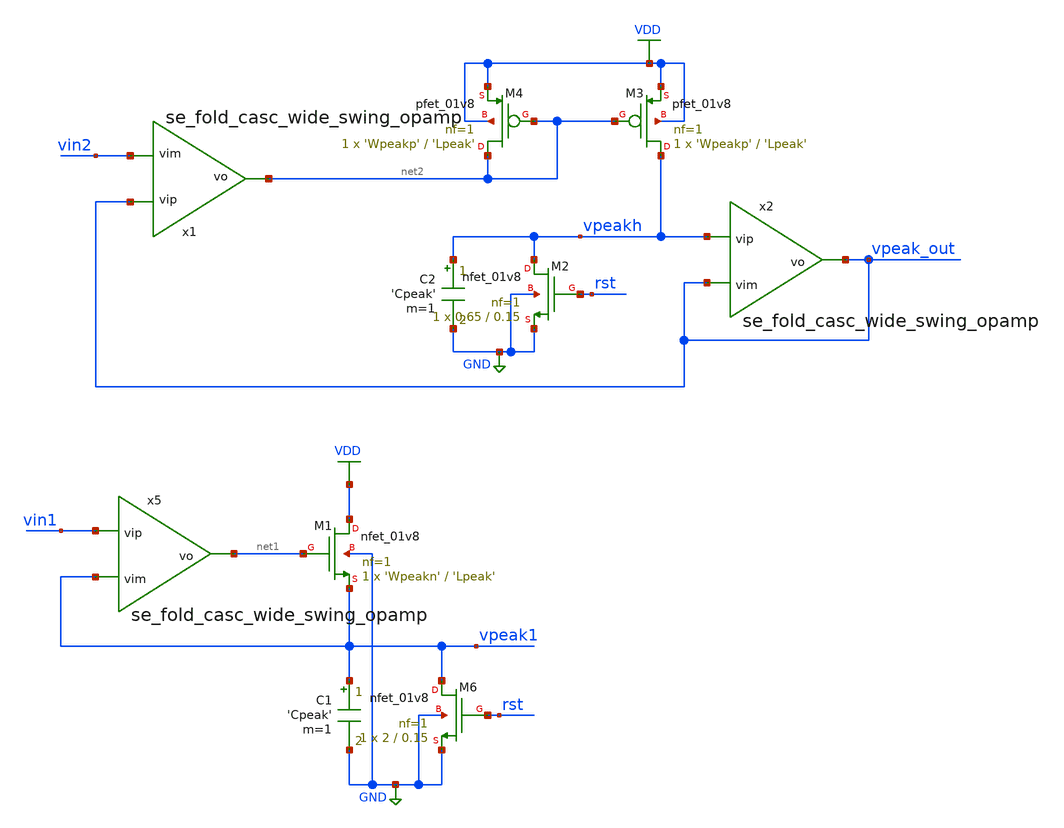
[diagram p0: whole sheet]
** sch_path: designs/peak_detector.sch
* Copyright 2020 Stefan Frederik Schippers
* Licensed under the Apache License, Version 2.0 (the "License");
* you may not use this file except in compliance with the License.
* You may obtain a copy of the License at
* https://www.apache.org/licenses/LICENSE-2.0
* Unless required by applicable law or agreed to in writing, software
* distributed under the License is distributed on an "AS IS" BASIS,
* WITHOUT WARRANTIES OR CONDITIONS OF ANY KIND, either express or implied.
* See the License for the specific language governing permissions and
* limitations under the License.
**.subckt peak_detector
x5 net1 vin1 vpeak1 se_fold_casc_wide_swing_opamp Lbias=6.4 Ibias=10u
C1 vpeak1 GND 'Cpeak' m=1
XM6 vpeak1 rst GND GND sky130_fd_pr__nfet_01v8 L=0.15 W=2 nf=1 ad='int((nf+1)/2) * W/nf * 0.29' as='int((nf+2)/2) * W/nf * 0.29'
+ pd='2*int((nf+1)/2) * (W/nf + 0.29)' ps='2*int((nf+2)/2) * (W/nf + 0.29)' nrd='0.29 / W' nrs='0.29 / W'
+ sa=0 sb=0 sd=0 mult=1 m=1
XM1 VDD net1 vpeak1 GND sky130_fd_pr__nfet_01v8 L='Lpeak' W='Wpeakn' nf=1 ad='int((nf+1)/2) * W/nf * 0.29'
+ as='int((nf+2)/2) * W/nf * 0.29' pd='2*int((nf+1)/2) * (W/nf + 0.29)' ps='2*int((nf+2)/2) * (W/nf + 0.29)'
+ nrd='0.29 / W' nrs='0.29 / W' sa=0 sb=0 sd=0 mult=1 m=1
x1 net2 vpeak_out vin2 se_fold_casc_wide_swing_opamp Lbias=6.4 Ibias=10u
C2 vpeakh GND 'Cpeak' m=1
XM3 vpeakh net2 VDD VDD sky130_fd_pr__pfet_01v8 L='Lpeak' W='Wpeakp' nf=1 ad='int((nf+1)/2) * W/nf * 0.29'
+ as='int((nf+2)/2) * W/nf * 0.29' pd='2*int((nf+1)/2) * (W/nf + 0.29)' ps='2*int((nf+2)/2) * (W/nf + 0.29)'
+ nrd='0.29 / W' nrs='0.29 / W' sa=0 sb=0 sd=0 mult=1 m=1
XM4 net2 net2 VDD VDD sky130_fd_pr__pfet_01v8 L='Lpeak' W='Wpeakp' nf=1 ad='int((nf+1)/2) * W/nf * 0.29'
+ as='int((nf+2)/2) * W/nf * 0.29' pd='2*int((nf+1)/2) * (W/nf + 0.29)' ps='2*int((nf+2)/2) * (W/nf + 0.29)'
+ nrd='0.29 / W' nrs='0.29 / W' sa=0 sb=0 sd=0 mult=1 m=1
x2 vpeak_out vpeakh vpeak_out se_fold_casc_wide_swing_opamp Lbias=6.4 Ibias=10u
XM2 vpeakh rst GND GND sky130_fd_pr__nfet_01v8 L=0.15 W=0.65 nf=1 ad='int((nf+1)/2) * W/nf * 0.29' as='int((nf+2)/2) * W/nf * 0.29'
+ pd='2*int((nf+1)/2) * (W/nf + 0.29)' ps='2*int((nf+2)/2) * (W/nf + 0.29)' nrd='0.29 / W' nrs='0.29 / W'
+ sa=0 sb=0 sd=0 mult=1 m=1
**** begin user architecture code

.include $::SKYWATER_MODELS/cells/nfet_01v8/sky130_fd_pr__nfet_01v8__tt.corner.spice
.include $::SKYWATER_MODELS/cells/nfet_01v8_lvt/sky130_fd_pr__nfet_01v8_lvt__tt.corner.spice
.include $::SKYWATER_MODELS/cells/pfet_01v8/sky130_fd_pr__pfet_01v8__tt.corner.spice
.include $::SKYWATER_MODELS/cells/nfet_03v3_nvt/sky130_fd_pr__nfet_03v3_nvt__tt.corner.spice
.include $::SKYWATER_MODELS/cells/nfet_05v0_nvt/sky130_fd_pr__nfet_05v0_nvt__tt.corner.spice
.include $::SKYWATER_MODELS/cells/esd_nfet_01v8/sky130_fd_pr__esd_nfet_01v8__tt.corner.spice
.include $::SKYWATER_MODELS/cells/pfet_01v8_lvt/sky130_fd_pr__pfet_01v8_lvt__tt.corner.spice
.include $::SKYWATER_MODELS/cells/pfet_01v8_hvt/sky130_fd_pr__pfet_01v8_hvt__tt.corner.spice
.include $::SKYWATER_MODELS/cells/esd_pfet_g5v0d10v5/sky130_fd_pr__esd_pfet_g5v0d10v5__tt.corner.spice
.include $::SKYWATER_MODELS/cells/pfet_g5v0d10v5/sky130_fd_pr__pfet_g5v0d10v5__tt.corner.spice
.include $::SKYWATER_MODELS/cells/pfet_g5v0d16v0/sky130_fd_pr__pfet_g5v0d16v0__tt.corner.spice
.include $::SKYWATER_MODELS/cells/nfet_g5v0d10v5/sky130_fd_pr__nfet_g5v0d10v5__tt.corner.spice
.include $::SKYWATER_MODELS/cells/nfet_g5v0d16v0/sky130_fd_pr__nfet_g5v0d16v0__tt_discrete.corner.spice
.include $::SKYWATER_MODELS/cells/esd_nfet_g5v0d10v5/sky130_fd_pr__esd_nfet_g5v0d10v5__tt.corner.spice
.include $::SKYWATER_MODELS/models/corners/tt/nonfet.spice
* Mismatch parameters
.include $::SKYWATER_MODELS/cells/nfet_01v8/sky130_fd_pr__nfet_01v8__mismatch.corner.spice
.include $::SKYWATER_MODELS/cells/pfet_01v8/sky130_fd_pr__pfet_01v8__mismatch.corner.spice
.include $::SKYWATER_MODELS/cells/nfet_01v8_lvt/sky130_fd_pr__nfet_01v8_lvt__mismatch.corner.spice
.include $::SKYWATER_MODELS/cells/pfet_01v8_lvt/sky130_fd_pr__pfet_01v8_lvt__mismatch.corner.spice
.include $::SKYWATER_MODELS/cells/pfet_01v8_hvt/sky130_fd_pr__pfet_01v8_hvt__mismatch.corner.spice
.include $::SKYWATER_MODELS/cells/nfet_g5v0d10v5/sky130_fd_pr__nfet_g5v0d10v5__mismatch.corner.spice
.include $::SKYWATER_MODELS/cells/pfet_g5v0d10v5/sky130_fd_pr__pfet_g5v0d10v5__mismatch.corner.spice
.include $::SKYWATER_MODELS/cells/nfet_05v0_nvt/sky130_fd_pr__nfet_05v0_nvt__mismatch.corner.spice
.include $::SKYWATER_MODELS/cells/nfet_03v3_nvt/sky130_fd_pr__nfet_03v3_nvt__mismatch.corner.spice
* Resistor$::SKYWATER_MODELS/Capacitor
.include $::SKYWATER_MODELS/models/r+c/res_typical__cap_typical.spice
.include $::SKYWATER_MODELS/models/r+c/res_typical__cap_typical__lin.spice
* Special cells
.include $::SKYWATER_MODELS/models/corners/tt/specialized_cells.spice
* All models
.include $::SKYWATER_MODELS/models/all.spice
* Corner
.include $::SKYWATER_MODELS/models/corners/tt/rf.spice

**** end user architecture code
**.ends

* expanding   symbol:
*+  /home/users/nhpoole/ee272b/ee272b_mixed_signal_mmwave_accelerator/designs/se_fold_casc_wide_swing_opamp.sym # of pins=3
** sym_path: designs/se_fold_casc_wide_swing_opamp.sym
** sch_path: designs/se_fold_casc_wide_swing_opamp.sch
.subckt se_fold_casc_wide_swing_opamp vo vip vim  Lbias=6.4 Ibias=10u
*.ipin vip
*.ipin vim
*.opin vo
V6 vtail_cascn net1 0
XM7 net1 vbias4 GND GND sky130_fd_pr__nfet_01v8 L='Lbias*nfactorL' W='Wbias*nfactorW' nf=1 ad='int((nf+1)/2) * W/nf * 0.29'
+ as='int((nf+2)/2) * W/nf * 0.29' pd='2*int((nf+1)/2) * (W/nf + 0.29)' ps='2*int((nf+2)/2) * (W/nf + 0.29)'
+ nrd='0.29 / W' nrs='0.29 / W' sa=0 sb=0 sd=0 mult='9*K' m='9*K'
XM10 vcascnp vbias4 GND GND sky130_fd_pr__nfet_01v8 L='Lbias*nfactorL' W='2*Wbias*nfactorW' nf=1 ad='int((nf+1)/2) * W/nf * 0.29'
+ as='int((nf+2)/2) * W/nf * 0.29' pd='2*int((nf+1)/2) * (W/nf + 0.29)' ps='2*int((nf+2)/2) * (W/nf + 0.29)'
+ nrd='0.29 / W' nrs='0.29 / W' sa=0 sb=0 sd=0 mult='9*K' m='9*K'
XM11 net11 vbias3 vcascnp GND sky130_fd_pr__nfet_01v8 L='Lbias*nfactorL' W='Wbias*nfactorW' nf=1 ad='int((nf+1)/2) * W/nf * 0.29'
+ as='int((nf+2)/2) * W/nf * 0.29' pd='2*int((nf+1)/2) * (W/nf + 0.29)' ps='2*int((nf+2)/2) * (W/nf + 0.29)'
+ nrd='0.29 / W' nrs='0.29 / W' sa=0 sb=0 sd=0 mult='9*K' m='9*K'
XM27 vcascnm vbias4 GND GND sky130_fd_pr__nfet_01v8 L='Lbias*nfactorL' W='2*Wbias*nfactorW' nf=1 ad='int((nf+1)/2) * W/nf * 0.29'
+ as='int((nf+2)/2) * W/nf * 0.29' pd='2*int((nf+1)/2) * (W/nf + 0.29)' ps='2*int((nf+2)/2) * (W/nf + 0.29)'
+ nrd='0.29 / W' nrs='0.29 / W' sa=0 sb=0 sd=0 mult='9*K' m='9*K'
XM28 vo vbias3 vcascnm GND sky130_fd_pr__nfet_01v8 L='Lbias*nfactorL' W='Wbias*nfactorW' nf=1 ad='int((nf+1)/2) * W/nf * 0.29'
+ as='int((nf+2)/2) * W/nf * 0.29' pd='2*int((nf+1)/2) * (W/nf + 0.29)' ps='2*int((nf+2)/2) * (W/nf + 0.29)'
+ nrd='0.29 / W' nrs='0.29 / W' sa=0 sb=0 sd=0 mult='9*K' m='9*K'
XM36 vbias1 vbias2 net7 VDD sky130_fd_pr__pfet_01v8 L='Lbias' W='2*Wbias' nf=1 ad='int((nf+1)/2) * W/nf * 0.29'
+ as='int((nf+2)/2) * W/nf * 0.29' pd='2*int((nf+1)/2) * (W/nf + 0.29)' ps='2*int((nf+2)/2) * (W/nf + 0.29)'
+ nrd='0.29 / W' nrs='0.29 / W' sa=0 sb=0 sd=0 mult='9*K' m='9*K'
XM37 net4 vbias2 net2 VDD sky130_fd_pr__pfet_01v8 L='Lbias' W='2*Wbias' nf=1 ad='int((nf+1)/2) * W/nf * 0.29'
+ as='int((nf+2)/2) * W/nf * 0.29' pd='2*int((nf+1)/2) * (W/nf + 0.29)' ps='2*int((nf+2)/2) * (W/nf + 0.29)'
+ nrd='0.29 / W' nrs='0.29 / W' sa=0 sb=0 sd=0 mult='9*K' m='9*K'
XM38 net6 vbias2 net5 VDD sky130_fd_pr__pfet_01v8 L='Lbias' W='2*Wbias' nf=1 ad='int((nf+1)/2) * W/nf * 0.29'
+ as='int((nf+2)/2) * W/nf * 0.29' pd='2*int((nf+1)/2) * (W/nf + 0.29)' ps='2*int((nf+2)/2) * (W/nf + 0.29)'
+ nrd='0.29 / W' nrs='0.29 / W' sa=0 sb=0 sd=0 mult='9*K' m='9*K'
XM39 vbias2 net3 vbias1 VDD sky130_fd_pr__pfet_01v8 L='Lbias' W='Wbias' nf=1 ad='int((nf+1)/2) * W/nf * 0.29'
+ as='int((nf+2)/2) * W/nf * 0.29' pd='2*int((nf+1)/2) * (W/nf + 0.29)' ps='2*int((nf+2)/2) * (W/nf + 0.29)'
+ nrd='0.29 / W' nrs='0.29 / W' sa=0 sb=0 sd=0 mult='3*K' m='3*K'
XM40 net3 net3 vbias2 VDD sky130_fd_pr__pfet_01v8 L='Lbias' W='3*Wbias' nf=1 ad='int((nf+1)/2) * W/nf * 0.29'
+ as='int((nf+2)/2) * W/nf * 0.29' pd='2*int((nf+1)/2) * (W/nf + 0.29)' ps='2*int((nf+2)/2) * (W/nf + 0.29)'
+ nrd='0.29 / W' nrs='0.29 / W' sa=0 sb=0 sd=0 mult='9*K' m='9*K'
XM41 net4 net4 vbias3 GND sky130_fd_pr__nfet_01v8 L='Lbias*nfactorL' W='3*Wbias*nfactorW' nf=1 ad='int((nf+1)/2) * W/nf * 0.29'
+ as='int((nf+2)/2) * W/nf * 0.29' pd='2*int((nf+1)/2) * (W/nf + 0.29)' ps='2*int((nf+2)/2) * (W/nf + 0.29)'
+ nrd='0.29 / W' nrs='0.29 / W' sa=0 sb=0 sd=0 mult='9*K' m='9*K'
XM42 vbias3 net4 vbias4 GND sky130_fd_pr__nfet_01v8 L='Lbias*nfactorL' W='Wbias*nfactorW' nf=1 ad='int((nf+1)/2) * W/nf * 0.29'
+ as='int((nf+2)/2) * W/nf * 0.29' pd='2*int((nf+1)/2) * (W/nf + 0.29)' ps='2*int((nf+2)/2) * (W/nf + 0.29)'
+ nrd='0.29 / W' nrs='0.29 / W' sa=0 sb=0 sd=0 mult='K' m='K'
XM43 vbias4 vbias3 net9 GND sky130_fd_pr__nfet_01v8 L='Lbias*nfactorL' W='Wbias*nfactorW' nf=1 ad='int((nf+1)/2) * W/nf * 0.29'
+ as='int((nf+2)/2) * W/nf * 0.29' pd='2*int((nf+1)/2) * (W/nf + 0.29)' ps='2*int((nf+2)/2) * (W/nf + 0.29)'
+ nrd='0.29 / W' nrs='0.29 / W' sa=0 sb=0 sd=0 mult='9*K' m='9*K'
XM44 net10 vbias4 GND GND sky130_fd_pr__nfet_01v8 L='Lbias*nfactorL' W='Wbias*nfactorW' nf=1 ad='int((nf+1)/2) * W/nf * 0.29'
+ as='int((nf+2)/2) * W/nf * 0.29' pd='2*int((nf+1)/2) * (W/nf + 0.29)' ps='2*int((nf+2)/2) * (W/nf + 0.29)'
+ nrd='0.29 / W' nrs='0.29 / W' sa=0 sb=0 sd=0 mult='9*K' m='9*K'
XM45 net6 net6 net8 net8 sky130_fd_pr__nfet_01v8 L='Lbias' W='0.6*Wbias' nf=1 ad='int((nf+1)/2) * W/nf * 0.29'
+ as='int((nf+2)/2) * W/nf * 0.29' pd='2*int((nf+1)/2) * (W/nf + 0.29)' ps='2*int((nf+2)/2) * (W/nf + 0.29)'
+ nrd='0.29 / W' nrs='0.29 / W' sa=0 sb=0 sd=0 mult='K' m='K'
I1 net3 GND 'Ibias'
V7 net8 GND 0
V8 net9 net10 0
XM12 net11 vbias2 vfoldp VDD sky130_fd_pr__pfet_01v8 L='Lbias' W='2*Wbias' nf=1 ad='int((nf+1)/2) * W/nf * 0.29'
+ as='int((nf+2)/2) * W/nf * 0.29' pd='2*int((nf+1)/2) * (W/nf + 0.29)' ps='2*int((nf+2)/2) * (W/nf + 0.29)'
+ nrd='0.29 / W' nrs='0.29 / W' sa=0 sb=0 sd=0 mult='9*K' m='9*K'
XM31 vo vbias2 vfoldm VDD sky130_fd_pr__pfet_01v8 L='Lbias' W='2*Wbias' nf=1 ad='int((nf+1)/2) * W/nf * 0.29'
+ as='int((nf+2)/2) * W/nf * 0.29' pd='2*int((nf+1)/2) * (W/nf + 0.29)' ps='2*int((nf+2)/2) * (W/nf + 0.29)'
+ nrd='0.29 / W' nrs='0.29 / W' sa=0 sb=0 sd=0 mult='9*K' m='9*K'
XM15 vfoldp net11 VDD VDD sky130_fd_pr__pfet_01v8_lvt L='Lbias' W='4*Wbias' nf=1 ad='int((nf+1)/2) * W/nf * 0.29'
+ as='int((nf+2)/2) * W/nf * 0.29' pd='2*int((nf+1)/2) * (W/nf + 0.29)' ps='2*int((nf+2)/2) * (W/nf + 0.29)'
+ nrd='0.29 / W' nrs='0.29 / W' sa=0 sb=0 sd=0 mult='9*K' m='9*K'
XM32 vfoldm net11 VDD VDD sky130_fd_pr__pfet_01v8_lvt L='Lbias' W='4*Wbias' nf=1 ad='int((nf+1)/2) * W/nf * 0.29'
+ as='int((nf+2)/2) * W/nf * 0.29' pd='2*int((nf+1)/2) * (W/nf + 0.29)' ps='2*int((nf+2)/2) * (W/nf + 0.29)'
+ nrd='0.29 / W' nrs='0.29 / W' sa=0 sb=0 sd=0 mult='9*K' m='9*K'
XM33 net7 vbias1 VDD VDD sky130_fd_pr__pfet_01v8_lvt L='Lbias' W='2*Wbias' nf=1 ad='int((nf+1)/2) * W/nf * 0.29'
+ as='int((nf+2)/2) * W/nf * 0.29' pd='2*int((nf+1)/2) * (W/nf + 0.29)' ps='2*int((nf+2)/2) * (W/nf + 0.29)'
+ nrd='0.29 / W' nrs='0.29 / W' sa=0 sb=0 sd=0 mult='9*K' m='9*K'
XM34 net2 vbias1 VDD VDD sky130_fd_pr__pfet_01v8_lvt L='Lbias' W='2*Wbias' nf=1 ad='int((nf+1)/2) * W/nf * 0.29'
+ as='int((nf+2)/2) * W/nf * 0.29' pd='2*int((nf+1)/2) * (W/nf + 0.29)' ps='2*int((nf+2)/2) * (W/nf + 0.29)'
+ nrd='0.29 / W' nrs='0.29 / W' sa=0 sb=0 sd=0 mult='9*K' m='9*K'
XM35 net5 vbias1 VDD VDD sky130_fd_pr__pfet_01v8_lvt L='Lbias' W='2*Wbias' nf=1 ad='int((nf+1)/2) * W/nf * 0.29'
+ as='int((nf+2)/2) * W/nf * 0.29' pd='2*int((nf+1)/2) * (W/nf + 0.29)' ps='2*int((nf+2)/2) * (W/nf + 0.29)'
+ nrd='0.29 / W' nrs='0.29 / W' sa=0 sb=0 sd=0 mult='9*K' m='9*K'
XM5 net1 vbias4 GND GND sky130_fd_pr__nfet_01v8 L='Lbias*nfactorL' W='Wbias*nfactorW' nf=1 ad='int((nf+1)/2) * W/nf * 0.29'
+ as='int((nf+2)/2) * W/nf * 0.29' pd='2*int((nf+1)/2) * (W/nf + 0.29)' ps='2*int((nf+2)/2) * (W/nf + 0.29)'
+ nrd='0.29 / W' nrs='0.29 / W' sa=0 sb=0 sd=0 mult='9*K' m='9*K'
XM6 net12 vbias1 VDD VDD sky130_fd_pr__pfet_01v8_lvt L='Lbias' W='2*Wbias' nf=1 ad='int((nf+1)/2) * W/nf * 0.29'
+ as='int((nf+2)/2) * W/nf * 0.29' pd='2*int((nf+1)/2) * (W/nf + 0.29)' ps='2*int((nf+2)/2) * (W/nf + 0.29)'
+ nrd='0.29 / W' nrs='0.29 / W' sa=0 sb=0 sd=0 mult='9*K' m='9*K'
V1 net12 vtail_cascp 0
XM13 net12 vbias1 VDD VDD sky130_fd_pr__pfet_01v8_lvt L='Lbias' W='2*Wbias' nf=1 ad='int((nf+1)/2) * W/nf * 0.29'
+ as='int((nf+2)/2) * W/nf * 0.29' pd='2*int((nf+1)/2) * (W/nf + 0.29)' ps='2*int((nf+2)/2) * (W/nf + 0.29)'
+ nrd='0.29 / W' nrs='0.29 / W' sa=0 sb=0 sd=0 mult='9*K' m='9*K'
XM2 vcascnm vim vtail_cascp VDD sky130_fd_pr__pfet_01v8_lvt L='Lbias' W='Wbias' nf=1 ad='int((nf+1)/2) * W/nf * 0.29'
+ as='int((nf+2)/2) * W/nf * 0.29' pd='2*int((nf+1)/2) * (W/nf + 0.29)' ps='2*int((nf+2)/2) * (W/nf + 0.29)'
+ nrd='0.29 / W' nrs='0.29 / W' sa=0 sb=0 sd=0 mult='6*K' m='6*K'
XM3 vcascnp vip vtail_cascp VDD sky130_fd_pr__pfet_01v8_lvt L='Lbias' W='Wbias' nf=1 ad='int((nf+1)/2) * W/nf * 0.29'
+ as='int((nf+2)/2) * W/nf * 0.29' pd='2*int((nf+1)/2) * (W/nf + 0.29)' ps='2*int((nf+2)/2) * (W/nf + 0.29)'
+ nrd='0.29 / W' nrs='0.29 / W' sa=0 sb=0 sd=0 mult='6*K' m='6*K'
XM17 net13 vbias4_ GND GND sky130_fd_pr__nfet_01v8 L='Lbias*nfactorL' W='Wbias*nfactorW' nf=1 ad='int((nf+1)/2) * W/nf * 0.29'
+ as='int((nf+2)/2) * W/nf * 0.29' pd='2*int((nf+1)/2) * (W/nf + 0.29)' ps='2*int((nf+2)/2) * (W/nf + 0.29)'
+ nrd='0.29 / W' nrs='0.29 / W' sa=0 sb=0 sd=0 mult='9*K' m='9*K'
XM18 vbias4_ vbias4_ GND GND sky130_fd_pr__nfet_01v8 L='Lbias*nfactorL' W='Wbias*nfactorW' nf=1 ad='int((nf+1)/2) * W/nf * 0.29'
+ as='int((nf+2)/2) * W/nf * 0.29' pd='2*int((nf+1)/2) * (W/nf + 0.29)' ps='2*int((nf+2)/2) * (W/nf + 0.29)'
+ nrd='0.29 / W' nrs='0.29 / W' sa=0 sb=0 sd=0 mult='9*K' m='9*K'
XM19 net15 net15 vbias4_ GND sky130_fd_pr__nfet_01v8 L='Lbias*nfactorL' W='Wbias*nfactorW' nf=1 ad='int((nf+1)/2) * W/nf * 0.29'
+ as='int((nf+2)/2) * W/nf * 0.29' pd='2*int((nf+1)/2) * (W/nf + 0.29)' ps='2*int((nf+2)/2) * (W/nf + 0.29)'
+ nrd='0.29 / W' nrs='0.29 / W' sa=0 sb=0 sd=0 mult='9*K' m='9*K'
XM20 net14 net15 net13 GND sky130_fd_pr__nfet_01v8 L='Lbias*nfactorL' W='Wbias*nfactorW' nf=1 ad='int((nf+1)/2) * W/nf * 0.29'
+ as='int((nf+2)/2) * W/nf * 0.29' pd='2*int((nf+1)/2) * (W/nf + 0.29)' ps='2*int((nf+2)/2) * (W/nf + 0.29)'
+ nrd='0.29 / W' nrs='0.29 / W' sa=0 sb=0 sd=0 mult='9*K' m='9*K'
I2 VDD net15 'Ibias'
XM25 net14 net14 vbias2_ VDD sky130_fd_pr__pfet_01v8 L='Lbias' W='2*Wbias' nf=1 ad='int((nf+1)/2) * W/nf * 0.29'
+ as='int((nf+2)/2) * W/nf * 0.29' pd='2*int((nf+1)/2) * (W/nf + 0.29)' ps='2*int((nf+2)/2) * (W/nf + 0.29)'
+ nrd='0.29 / W' nrs='0.29 / W' sa=0 sb=0 sd=0 mult='9*K' m='9*K'
XM26 vbias2_ net14 VDD VDD sky130_fd_pr__pfet_01v8_lvt L='Lbias' W='4*Wbias' nf=1 ad='int((nf+1)/2) * W/nf * 0.29'
+ as='int((nf+2)/2) * W/nf * 0.29' pd='2*int((nf+1)/2) * (W/nf + 0.29)' ps='2*int((nf+2)/2) * (W/nf + 0.29)'
+ nrd='0.29 / W' nrs='0.29 / W' sa=0 sb=0 sd=0 mult='9*K' m='9*K'
XM21 vbias3_ net17 GND GND sky130_fd_pr__nfet_01v8 L='Lbias*nfactorL' W='Wbias*nfactorW' nf=1 ad='int((nf+1)/2) * W/nf * 0.29'
+ as='int((nf+2)/2) * W/nf * 0.29' pd='2*int((nf+1)/2) * (W/nf + 0.29)' ps='2*int((nf+2)/2) * (W/nf + 0.29)'
+ nrd='0.29 / W' nrs='0.29 / W' sa=0 sb=0 sd=0 mult='9*K' m='9*K'
XM22 net16 vbias4_ GND GND sky130_fd_pr__nfet_01v8 L='Lbias*nfactorL' W='Wbias*nfactorW' nf=1 ad='int((nf+1)/2) * W/nf * 0.29'
+ as='int((nf+2)/2) * W/nf * 0.29' pd='2*int((nf+1)/2) * (W/nf + 0.29)' ps='2*int((nf+2)/2) * (W/nf + 0.29)'
+ nrd='0.29 / W' nrs='0.29 / W' sa=0 sb=0 sd=0 mult='9*K' m='9*K'
XM23 net19 net15 net16 GND sky130_fd_pr__nfet_01v8 L='Lbias*nfactorL' W='Wbias*nfactorW' nf=1 ad='int((nf+1)/2) * W/nf * 0.29'
+ as='int((nf+2)/2) * W/nf * 0.29' pd='2*int((nf+1)/2) * (W/nf + 0.29)' ps='2*int((nf+2)/2) * (W/nf + 0.29)'
+ nrd='0.29 / W' nrs='0.29 / W' sa=0 sb=0 sd=0 mult='9*K' m='9*K'
XM24 net17 net17 vbias3_ GND sky130_fd_pr__nfet_01v8 L='Lbias*nfactorL' W='Wbias*nfactorW' nf=1 ad='int((nf+1)/2) * W/nf * 0.29'
+ as='int((nf+2)/2) * W/nf * 0.29' pd='2*int((nf+1)/2) * (W/nf + 0.29)' ps='2*int((nf+2)/2) * (W/nf + 0.29)'
+ nrd='0.29 / W' nrs='0.29 / W' sa=0 sb=0 sd=0 mult='9*K' m='9*K'
XM29 net17 net19 net18 VDD sky130_fd_pr__pfet_01v8 L='Lbias' W='2*Wbias' nf=1 ad='int((nf+1)/2) * W/nf * 0.29'
+ as='int((nf+2)/2) * W/nf * 0.29' pd='2*int((nf+1)/2) * (W/nf + 0.29)' ps='2*int((nf+2)/2) * (W/nf + 0.29)'
+ nrd='0.29 / W' nrs='0.29 / W' sa=0 sb=0 sd=0 mult='9*K' m='9*K'
XM30 net18 vbias1_ VDD VDD sky130_fd_pr__pfet_01v8_lvt L='Lbias' W='4*Wbias' nf=1 ad='int((nf+1)/2) * W/nf * 0.29'
+ as='int((nf+2)/2) * W/nf * 0.29' pd='2*int((nf+1)/2) * (W/nf + 0.29)' ps='2*int((nf+2)/2) * (W/nf + 0.29)'
+ nrd='0.29 / W' nrs='0.29 / W' sa=0 sb=0 sd=0 mult='9*K' m='9*K'
XM46 net19 net19 vbias1_ VDD sky130_fd_pr__pfet_01v8 L='Lbias' W='2*Wbias' nf=1 ad='int((nf+1)/2) * W/nf * 0.29'
+ as='int((nf+2)/2) * W/nf * 0.29' pd='2*int((nf+1)/2) * (W/nf + 0.29)' ps='2*int((nf+2)/2) * (W/nf + 0.29)'
+ nrd='0.29 / W' nrs='0.29 / W' sa=0 sb=0 sd=0 mult='9*K' m='9*K'
XM47 vbias1_ vbias1_ VDD VDD sky130_fd_pr__pfet_01v8_lvt L='Lbias' W='4*Wbias' nf=1 ad='int((nf+1)/2) * W/nf * 0.29'
+ as='int((nf+2)/2) * W/nf * 0.29' pd='2*int((nf+1)/2) * (W/nf + 0.29)' ps='2*int((nf+2)/2) * (W/nf + 0.29)'
+ nrd='0.29 / W' nrs='0.29 / W' sa=0 sb=0 sd=0 mult='9*K' m='9*K'
C2 vo GND 4p m=1
XM1 vfoldp vip vtail_cascn GND sky130_fd_pr__nfet_01v8_lvt L='K2*Lbias*nfactorL' W='Wbias*nfactorW' nf=1
+ ad='int((nf+1)/2) * W/nf * 0.29' as='int((nf+2)/2) * W/nf * 0.29' pd='2*int((nf+1)/2) * (W/nf + 0.29)'
+ ps='2*int((nf+2)/2) * (W/nf + 0.29)' nrd='0.29 / W' nrs='0.29 / W' sa=0 sb=0 sd=0 mult='9*K' m='9*K'
XM4 vfoldm vim vtail_cascn GND sky130_fd_pr__nfet_01v8_lvt L='K2*Lbias*nfactorL' W='Wbias*nfactorW' nf=1
+ ad='int((nf+1)/2) * W/nf * 0.29' as='int((nf+2)/2) * W/nf * 0.29' pd='2*int((nf+1)/2) * (W/nf + 0.29)'
+ ps='2*int((nf+2)/2) * (W/nf + 0.29)' nrd='0.29 / W' nrs='0.29 / W' sa=0 sb=0 sd=0 mult='9*K' m='9*K'
.ends

.GLOBAL GND
.GLOBAL VDD
**** begin user architecture code

.include peak_detector_commands.spice

**** end user architecture code
.end
